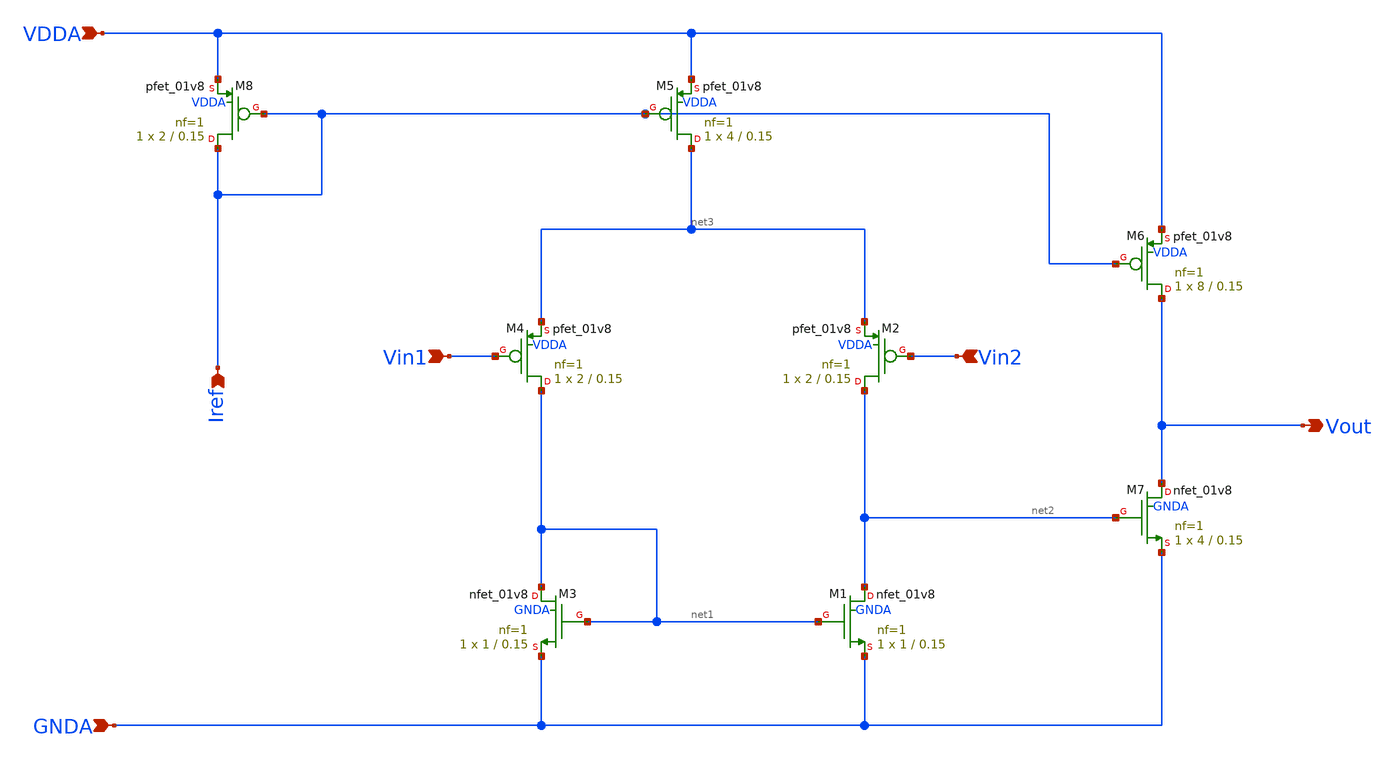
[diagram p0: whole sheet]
** sch_path: projects/pll/trials/opamp_trial.sch
**.subckt opamp_trial Vin1 Vin2 Iref Vout VDDA GNDA
*.ipin Vin1
*.ipin Vin2
*.ipin Iref
*.opin Vout
*.ipin VDDA
*.ipin GNDA
XM1 net2 net1 GNDA GNDA sky130_fd_pr__nfet_01v8 L=0.15 W=1 nf=1 ad='int((nf+1)/2) * W/nf * 0.29' as='int((nf+2)/2) * W/nf * 0.29'
+ pd='2*int((nf+1)/2) * (W/nf + 0.29)' ps='2*int((nf+2)/2) * (W/nf + 0.29)' nrd='0.29 / W' nrs='0.29 / W'
+ sa=0 sb=0 sd=0 mult=1 m=1
XM2 net2 Vin2 net3 VDDA sky130_fd_pr__pfet_01v8 L=0.15 W=2 nf=1 ad='int((nf+1)/2) * W/nf * 0.29' as='int((nf+2)/2) * W/nf * 0.29'
+ pd='2*int((nf+1)/2) * (W/nf + 0.29)' ps='2*int((nf+2)/2) * (W/nf + 0.29)' nrd='0.29 / W' nrs='0.29 / W'
+ sa=0 sb=0 sd=0 mult=1 m=1
XM3 net1 net1 GNDA GNDA sky130_fd_pr__nfet_01v8 L=0.15 W=1 nf=1 ad='int((nf+1)/2) * W/nf * 0.29' as='int((nf+2)/2) * W/nf * 0.29'
+ pd='2*int((nf+1)/2) * (W/nf + 0.29)' ps='2*int((nf+2)/2) * (W/nf + 0.29)' nrd='0.29 / W' nrs='0.29 / W'
+ sa=0 sb=0 sd=0 mult=1 m=1
XM4 net1 Vin1 net3 VDDA sky130_fd_pr__pfet_01v8 L=0.15 W=2 nf=1 ad='int((nf+1)/2) * W/nf * 0.29' as='int((nf+2)/2) * W/nf * 0.29'
+ pd='2*int((nf+1)/2) * (W/nf + 0.29)' ps='2*int((nf+2)/2) * (W/nf + 0.29)' nrd='0.29 / W' nrs='0.29 / W'
+ sa=0 sb=0 sd=0 mult=1 m=1
XM5 net3 Iref VDDA VDDA sky130_fd_pr__pfet_01v8 L=0.15 W=4 nf=1 ad='int((nf+1)/2) * W/nf * 0.29' as='int((nf+2)/2) * W/nf * 0.29'
+ pd='2*int((nf+1)/2) * (W/nf + 0.29)' ps='2*int((nf+2)/2) * (W/nf + 0.29)' nrd='0.29 / W' nrs='0.29 / W'
+ sa=0 sb=0 sd=0 mult=1 m=1
XM6 Vout Iref VDDA VDDA sky130_fd_pr__pfet_01v8 L=0.15 W=8 nf=1 ad='int((nf+1)/2) * W/nf * 0.29' as='int((nf+2)/2) * W/nf * 0.29'
+ pd='2*int((nf+1)/2) * (W/nf + 0.29)' ps='2*int((nf+2)/2) * (W/nf + 0.29)' nrd='0.29 / W' nrs='0.29 / W'
+ sa=0 sb=0 sd=0 mult=1 m=1
XM7 Vout net2 GNDA GNDA sky130_fd_pr__nfet_01v8 L=0.15 W=4 nf=1 ad='int((nf+1)/2) * W/nf * 0.29' as='int((nf+2)/2) * W/nf * 0.29'
+ pd='2*int((nf+1)/2) * (W/nf + 0.29)' ps='2*int((nf+2)/2) * (W/nf + 0.29)' nrd='0.29 / W' nrs='0.29 / W'
+ sa=0 sb=0 sd=0 mult=1 m=1
XM8 Iref Iref VDDA VDDA sky130_fd_pr__pfet_01v8 L=0.15 W=2 nf=1 ad='int((nf+1)/2) * W/nf * 0.29' as='int((nf+2)/2) * W/nf * 0.29'
+ pd='2*int((nf+1)/2) * (W/nf + 0.29)' ps='2*int((nf+2)/2) * (W/nf + 0.29)' nrd='0.29 / W' nrs='0.29 / W'
+ sa=0 sb=0 sd=0 mult=1 m=1
**.ends
.end
